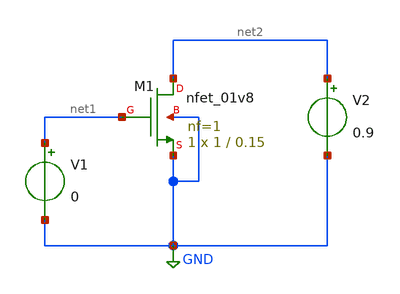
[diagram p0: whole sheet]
** sch_path: mySAR_SKY130/xschem/test/mosfet_test.sch
**.subckt mosfet_test
XM1 net2 net1 GND GND sky130_fd_pr__nfet_01v8 L=0.15 W=1 nf=1 ad='int((nf+1)/2) * W/nf * 0.29' as='int((nf+2)/2) * W/nf * 0.29'
+ pd='2*int((nf+1)/2) * (W/nf + 0.29)' ps='2*int((nf+2)/2) * (W/nf + 0.29)' nrd='0.29 / W' nrs='0.29 / W'
+ sa=0 sb=0 sd=0 mult=1 m=1
V1 net1 GND 0
V2 net2 GND 0.9
**** begin user architecture code



.lib /foss/pdks/sky130A/libs.tech/ngspice/sky130.lib.spice tt

.control
	dc V1 0 3 0.01
	plot -i(V2)

.endc

.save all



**** end user architecture code
**.ends
.GLOBAL GND
.end
